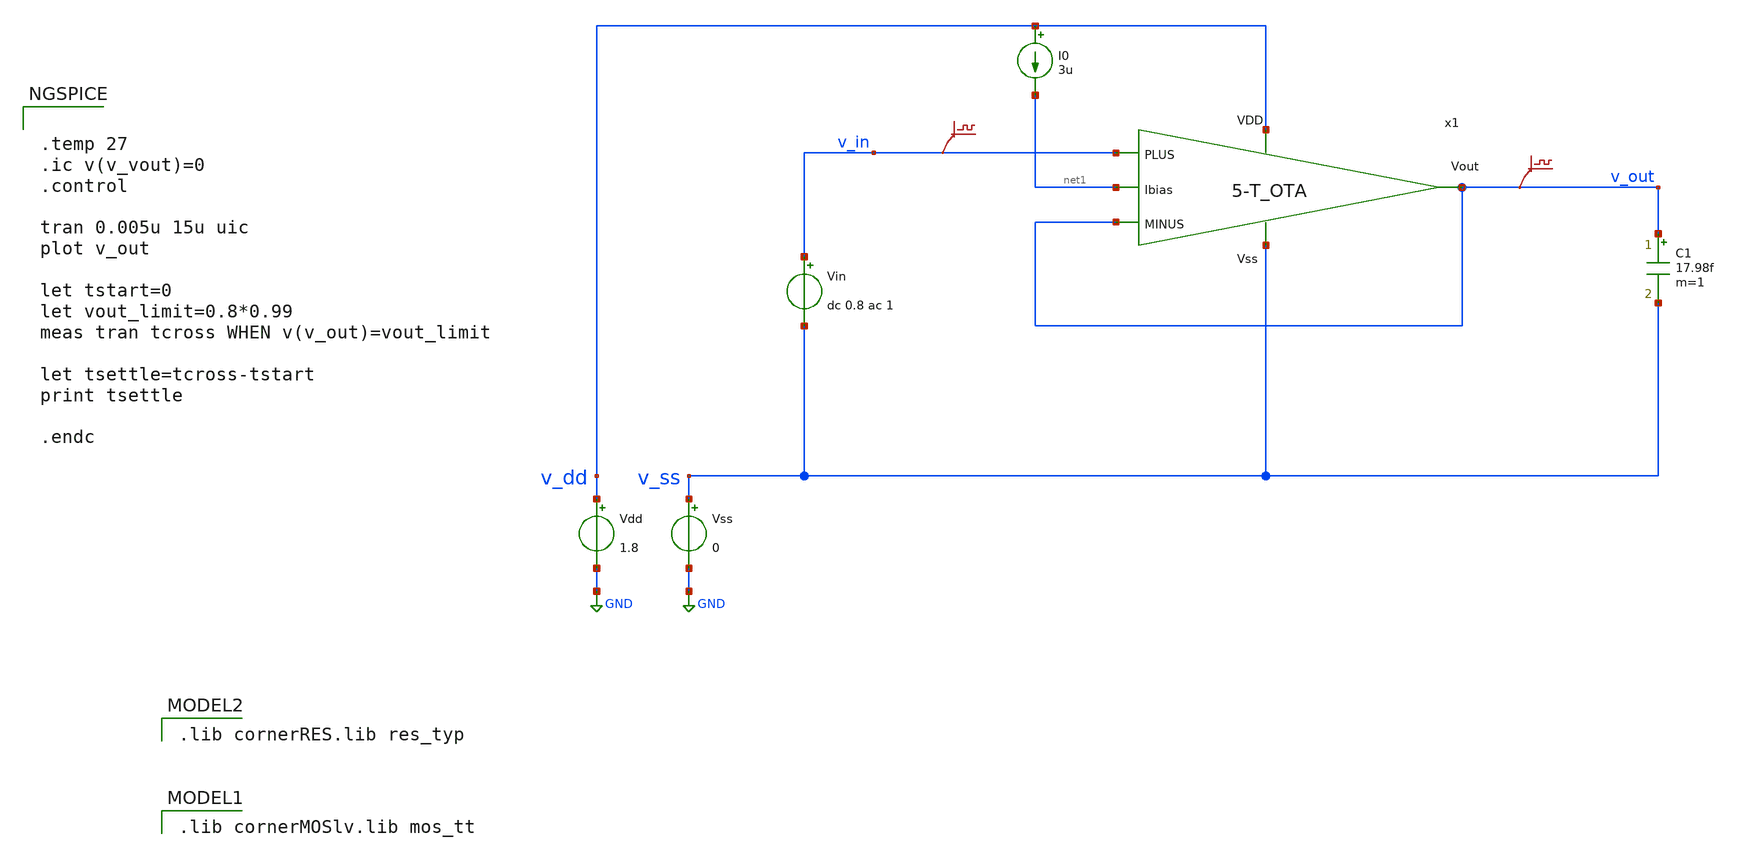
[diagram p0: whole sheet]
** sch_path: DSM/Schematics/IC_Designs_Hrishi/RealCircuits/5-T_OTA/tb_5-T_OTA_tran-1.sch
* (c) 2024 Hrishikesh, @HSB
**.subckt tb_5-T_OTA_tran-1
Vdd v_dd GND 1.8
Vss v_ss GND 0
C1 v_out v_ss 17.98f m=1
Vin v_in v_ss dc 0.8 ac 1
I0 v_dd net1 3u
.save v(v_in)
.save v(v_out)
x1 v_dd net1 v_out v_in v_out v_ss 5-T_OTA
**** begin user architecture code
 .lib cornerMOSlv.lib mos_tt

 .lib cornerRES.lib res_typ



.temp 27
.ic v(v_vout)=0
.control

tran 0.005u 15u uic
plot v_out

let tstart=0
let vout_limit=0.8*0.99
meas tran tcross WHEN v(v_out)=vout_limit

let tsettle=tcross-tstart
print tsettle

.endc


**** end user architecture code
**.ends

* expanding   symbol:
*+  /foss/designs/SecondOrder_SingleBit_DSM/DSM/IC_Designs_Hrishi/RealCircuits/5-T_OTA/5-T_OTA.sym # of pins=6
** sym_path: DSM/Schematics/Designs_Hrishi/RealCircuits/5-T_OTA/5-T_OTA.sym
** sch_path: DSM/Schematics/Designs_Hrishi/RealCircuits/5-T_OTA/5-T_OTA.sch
.subckt 5-T_OTA VDD Ibias Vout PLUS MINUS Vss
*.ipin MINUS
*.ipin PLUS
*.ipin VDD
*.ipin Ibias
*.ipin Vss
*.opin Vout
XM10 Vout net1 VDD VDD sg13_lv_pmos w=0.136u l=0.5u ng=1 m=1 mm_ok=1
XM11 net1 net1 VDD VDD sg13_lv_pmos w=0.136u l=0.5u ng=1 m=1 mm_ok=1
XM12 net1 PLUS net2 Vss sg13_lv_nmos w=0.15u l=2u ng=1 m=1 mm_ok=1
XM13 Vout MINUS net2 Vss sg13_lv_nmos w=0.15u l=2u ng=1 m=1 mm_ok=1
XM14 net2 net4 Vss Vss sg13_lv_nmos w=0.30u l=2u ng=1 m=1 mm_ok=1
XM1 net3 net4 Vss Vss sg13_lv_nmos w=0.15u l=2u ng=1 m=1 mm_ok=1
XM2 VDD VDD net3 Vss sg13_lv_nmos w=0.15u l=2u ng=1 m=1 mm_ok=1
XM3 net4 net4 Vss Vss sg13_lv_nmos w=0.15u l=2u ng=1 m=1 mm_ok=1
XM4 Ibias VDD net4 Vss sg13_lv_nmos w=0.15u l=2u ng=1 m=1 mm_ok=1
.ends

.GLOBAL GND
.end
